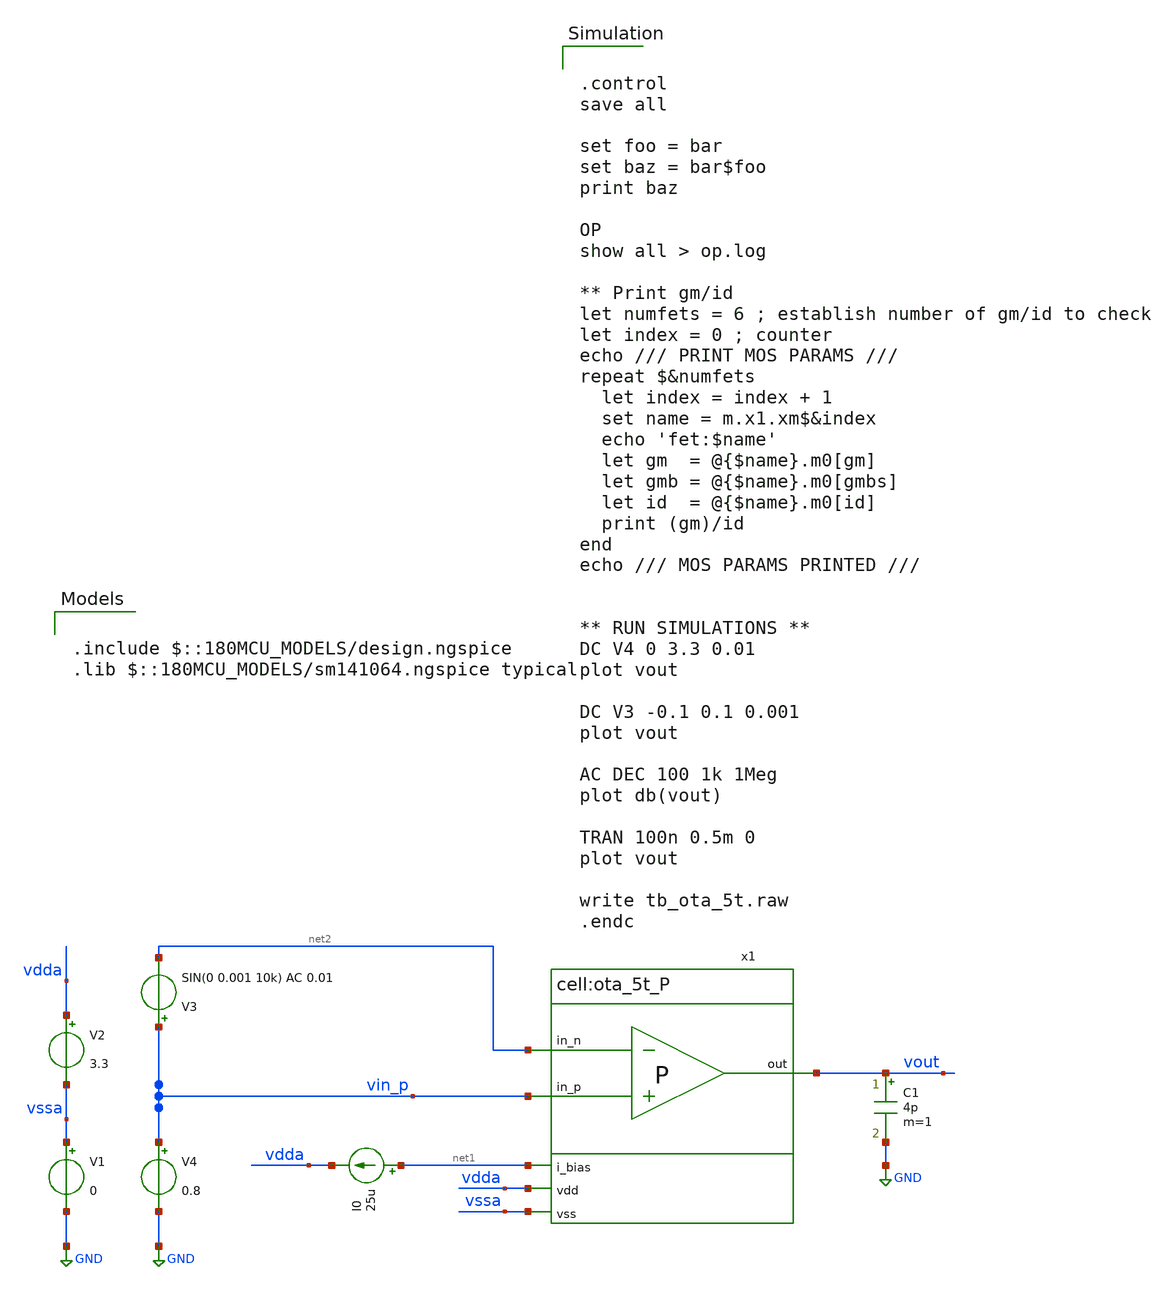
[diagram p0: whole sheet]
** sch_path: designs/libs/tb_analog/tb_ota_5t_dc/tb_ota_5t_p_dc.sch
**.subckt tb_ota_5t_p_dc
V1 vssa GND 0
V2 vdda vssa 3.3
I0 net1 vdda 25u
V3 vin_p net2 SIN(0 0.001 10k) AC 0.01
V4 vin_p GND 0.8
C1 vout GND 4p m=1
x1 vdda vout vin_p net2 net1 vssa ota_5t_P
**** begin user architecture code


.control
save all

set foo = bar
set baz = bar$foo
print baz

OP
show all > op.log

** Print gm/id
let numfets = 6 ; establish number of gm/id to check
let index = 0 ; counter
echo /// PRINT MOS PARAMS ///
repeat $&numfets
  let index = index + 1
  set name = m.x1.xm$&index
  echo 'fet:$name'
  let gm  = @{$name}.m0[gm]
  let gmb = @{$name}.m0[gmbs]
  let id  = @{$name}.m0[id]
  print (gm)/id
end
echo /// MOS PARAMS PRINTED ///


** RUN SIMULATIONS **
DC V4 0 3.3 0.01
plot vout

DC V3 -0.1 0.1 0.001
plot vout

AC DEC 100 1k 1Meg
plot db(vout)

TRAN 100n 0.5m 0
plot vout

write tb_ota_5t.raw
.endc



.include $::180MCU_MODELS/design.ngspice
.lib $::180MCU_MODELS/sm141064.ngspice typical

**** end user architecture code
**.ends

* expanding   symbol:  libs/core_analog/ota_5t/ota_5t_P.sym # of pins=6
** sym_path: libs/core_analog/ota_5t/ota_5t_P.sym
** sch_path: libs/core_analog/ota_5t/ota_5t_P.sch
.subckt ota_5t_P vdd out in_p in_n i_bias vss
*.ipin in_n
*.ipin i_bias
*.ipin vdd
*.ipin vss
*.opin out
*.ipin in_p
XM4 out net1 vss vss nfet_03v3 L=1u W=1.5u nf=1 ad='int((nf+1)/2) * W/nf * 0.18u' as='int((nf+2)/2) * W/nf * 0.18u'
+ pd='2*int((nf+1)/2) * (W/nf + 0.18u)' ps='2*int((nf+2)/2) * (W/nf + 0.18u)' nrd='0.18u / W' nrs='0.18u / W'
+ sa=0 sb=0 sd=0 m=1
XM3 net1 net1 vss vss nfet_03v3 L=1u W=1.5u nf=1 ad='int((nf+1)/2) * W/nf * 0.18u' as='int((nf+2)/2) * W/nf * 0.18u'
+ pd='2*int((nf+1)/2) * (W/nf + 0.18u)' ps='2*int((nf+2)/2) * (W/nf + 0.18u)' nrd='0.18u / W' nrs='0.18u / W'
+ sa=0 sb=0 sd=0 m=1
XM2 out in_n net2 vdd pfet_03v3 L=0.7u W=4u nf=3 ad='int((nf+1)/2) * W/nf * 0.18u' as='int((nf+2)/2) * W/nf * 0.18u'
+ pd='2*int((nf+1)/2) * (W/nf + 0.18u)' ps='2*int((nf+2)/2) * (W/nf + 0.18u)' nrd='0.18u / W' nrs='0.18u / W'
+ sa=0 sb=0 sd=0 m=3
XM1 net1 in_p net2 vdd pfet_03v3 L=0.7u W=4u nf=3 ad='int((nf+1)/2) * W/nf * 0.18u' as='int((nf+2)/2) * W/nf * 0.18u'
+ pd='2*int((nf+1)/2) * (W/nf + 0.18u)' ps='2*int((nf+2)/2) * (W/nf + 0.18u)' nrd='0.18u / W' nrs='0.18u / W'
+ sa=0 sb=0 sd=0 m=3
x2 vdd vdd i_bias i_bias unit_pmos M=1
x1 vdd vdd i_bias net2 unit_pmos M=1
.ends


* expanding   symbol:  libs/core_analog/unit_pmos/unit_pmos.sym # of pins=4
** sym_path: libs/core_analog/unit_pmos/unit_pmos.sym
** sch_path: libs/core_analog/unit_pmos/unit_pmos.sch
.subckt unit_pmos drain sub gate source
*.iopin drain
*.iopin source
*.iopin sub
*.iopin gate
**** begin user architecture code

.param M=1

**** end user architecture code
XM3 drain gate source sub pfet_03v3 L=1u W=3.5u nf=1 ad='int((nf+1)/2) * W/nf * 0.18u' as='int((nf+2)/2) * W/nf * 0.18u'
+ pd='2*int((nf+1)/2) * (W/nf + 0.18u)' ps='2*int((nf+2)/2) * (W/nf + 0.18u)' nrd='0.18u / W' nrs='0.18u / W'
+ sa=0 sb=0 sd=0 m={M}
.ends

.GLOBAL GND
.end
